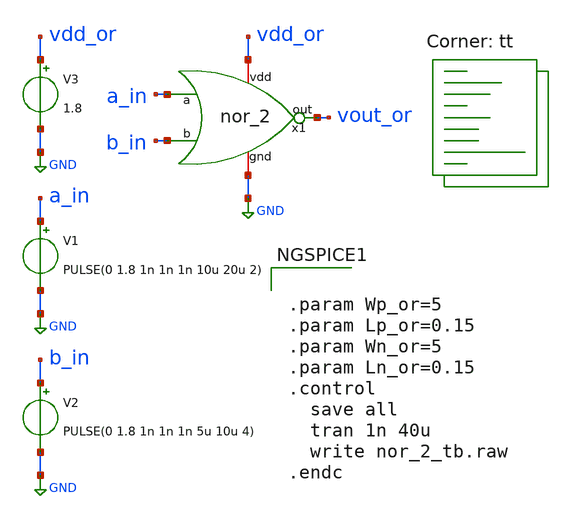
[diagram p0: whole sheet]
** sch_path: inhibitory/nor_2_tb.sch
**.subckt nor_2_tb
V1 a_in GND PULSE(0 1.8 1n 1n 1n 10u 20u 2)
V3 vdd_or GND 1.8
V2 b_in GND PULSE(0 1.8 1n 1n 1n 5u 10u 4)
x1 vdd_or vout_or a_in b_in GND nor_2
**** begin user architecture code
.lib $::SKYWATER_MODELS/sky130.lib.spice tt


.param Wp_or=5
.param Lp_or=0.15
.param Wn_or=5
.param Ln_or=0.15
.control
  save all
  tran 1n 40u
  write nor_2_tb.raw
.endc

**** end user architecture code
**.ends

* expanding   symbol:  /home/ricardo/RATT_repos/Proyectos_xschem/inhibitory/nor_2.sym # of pins=5
** sym_path: inhibitory/nor_2.sym
** sch_path: inhibitory/nor_2.sch
.subckt nor_2 vdd out a b gnd
*.iopin gnd
*.ipin a
*.ipin b
*.opin out
*.iopin vdd
XM1 net1 a vdd vdd sky130_fd_pr__pfet_01v8 L={Lp_or} W={Wp_or} nf=1 ad='int((nf+1)/2) * W/nf * 0.29'
+ as='int((nf+2)/2) * W/nf * 0.29' pd='2*int((nf+1)/2) * (W/nf + 0.29)' ps='2*int((nf+2)/2) * (W/nf + 0.29)'
+ nrd='0.29 / W' nrs='0.29 / W' sa=0 sb=0 sd=0 mult=1 m=1
XM2 out b gnd gnd sky130_fd_pr__nfet_01v8 L={Ln_or} W={Wn_or} nf=1 ad='int((nf+1)/2) * W/nf * 0.29' as='int((nf+2)/2) * W/nf * 0.29'
+ pd='2*int((nf+1)/2) * (W/nf + 0.29)' ps='2*int((nf+2)/2) * (W/nf + 0.29)' nrd='0.29 / W' nrs='0.29 / W'
+ sa=0 sb=0 sd=0 mult=1 m=1
XM3 out b net1 vdd sky130_fd_pr__pfet_01v8 L={Lp_or} W={Wp_or} nf=1 ad='int((nf+1)/2) * W/nf * 0.29'
+ as='int((nf+2)/2) * W/nf * 0.29' pd='2*int((nf+1)/2) * (W/nf + 0.29)' ps='2*int((nf+2)/2) * (W/nf + 0.29)'
+ nrd='0.29 / W' nrs='0.29 / W' sa=0 sb=0 sd=0 mult=1 m=1
XM4 out a gnd gnd sky130_fd_pr__nfet_01v8 L={Ln_or} W={Wn_or} nf=1 ad='int((nf+1)/2) * W/nf * 0.29' as='int((nf+2)/2) * W/nf * 0.29'
+ pd='2*int((nf+1)/2) * (W/nf + 0.29)' ps='2*int((nf+2)/2) * (W/nf + 0.29)' nrd='0.29 / W' nrs='0.29 / W'
+ sa=0 sb=0 sd=0 mult=1 m=1
.ends

.GLOBAL GND
.end
